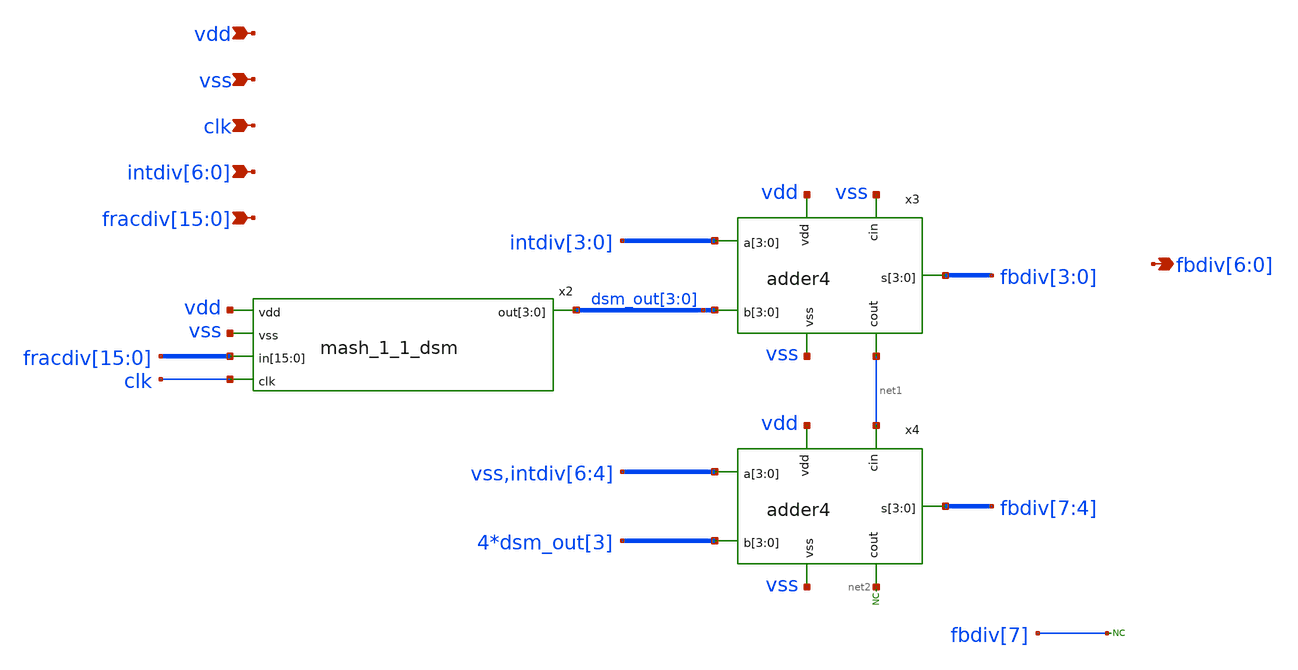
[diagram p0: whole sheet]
** sch_path: xschem/dsm.sch
**.subckt dsm vdd vss clk intdiv[6],intdiv[5],intdiv[4],intdiv[3],intdiv[2],intdiv[1],intdiv[0]
*+ fracdiv[15],fracdiv[14],fracdiv[13],fracdiv[12],fracdiv[11],fracdiv[10],fracdiv[9],fracdiv[8],fracdiv[7],fracdiv[6],fracdiv[5],fracdiv[4],fracdiv[3],fracdiv[2],fracdiv[1],fracdiv[0] fbdiv[6],fbdiv[5],fbdiv[4],fbdiv[3],fbdiv[2],fbdiv[1],fbdiv[0]
*.ipin vdd
*.ipin vss
*.ipin clk
*.ipin intdiv[6],intdiv[5],intdiv[4],intdiv[3],intdiv[2],intdiv[1],intdiv[0]
*.ipin
*+ fracdiv[15],fracdiv[14],fracdiv[13],fracdiv[12],fracdiv[11],fracdiv[10],fracdiv[9],fracdiv[8],fracdiv[7],fracdiv[6],fracdiv[5],fracdiv[4],fracdiv[3],fracdiv[2],fracdiv[1],fracdiv[0]
*.opin fbdiv[6],fbdiv[5],fbdiv[4],fbdiv[3],fbdiv[2],fbdiv[1],fbdiv[0]
x2 vdd vss fracdiv[15] fracdiv[14] fracdiv[13] fracdiv[12] fracdiv[11] fracdiv[10] fracdiv[9]
+ fracdiv[8] fracdiv[7] fracdiv[6] fracdiv[5] fracdiv[4] fracdiv[3] fracdiv[2] fracdiv[1] fracdiv[0] clk
+ dsm_out[3] dsm_out[2] dsm_out[1] dsm_out[0] mash_1_1_dsm
x3 vss vdd vss intdiv[3] intdiv[2] intdiv[1] intdiv[0] dsm_out[3] dsm_out[2] dsm_out[1] dsm_out[0]
+ fbdiv[3] fbdiv[2] fbdiv[1] fbdiv[0] net1 adder4
x4 net1 vdd vss vss intdiv[6] intdiv[5] intdiv[4] dsm_out[3] dsm_out[3] dsm_out[3] dsm_out[3]
+ fbdiv[7] fbdiv[6] fbdiv[5] fbdiv[4] net2 adder4
* noconn #net2
* noconn fbdiv[7]
**.ends
.end
